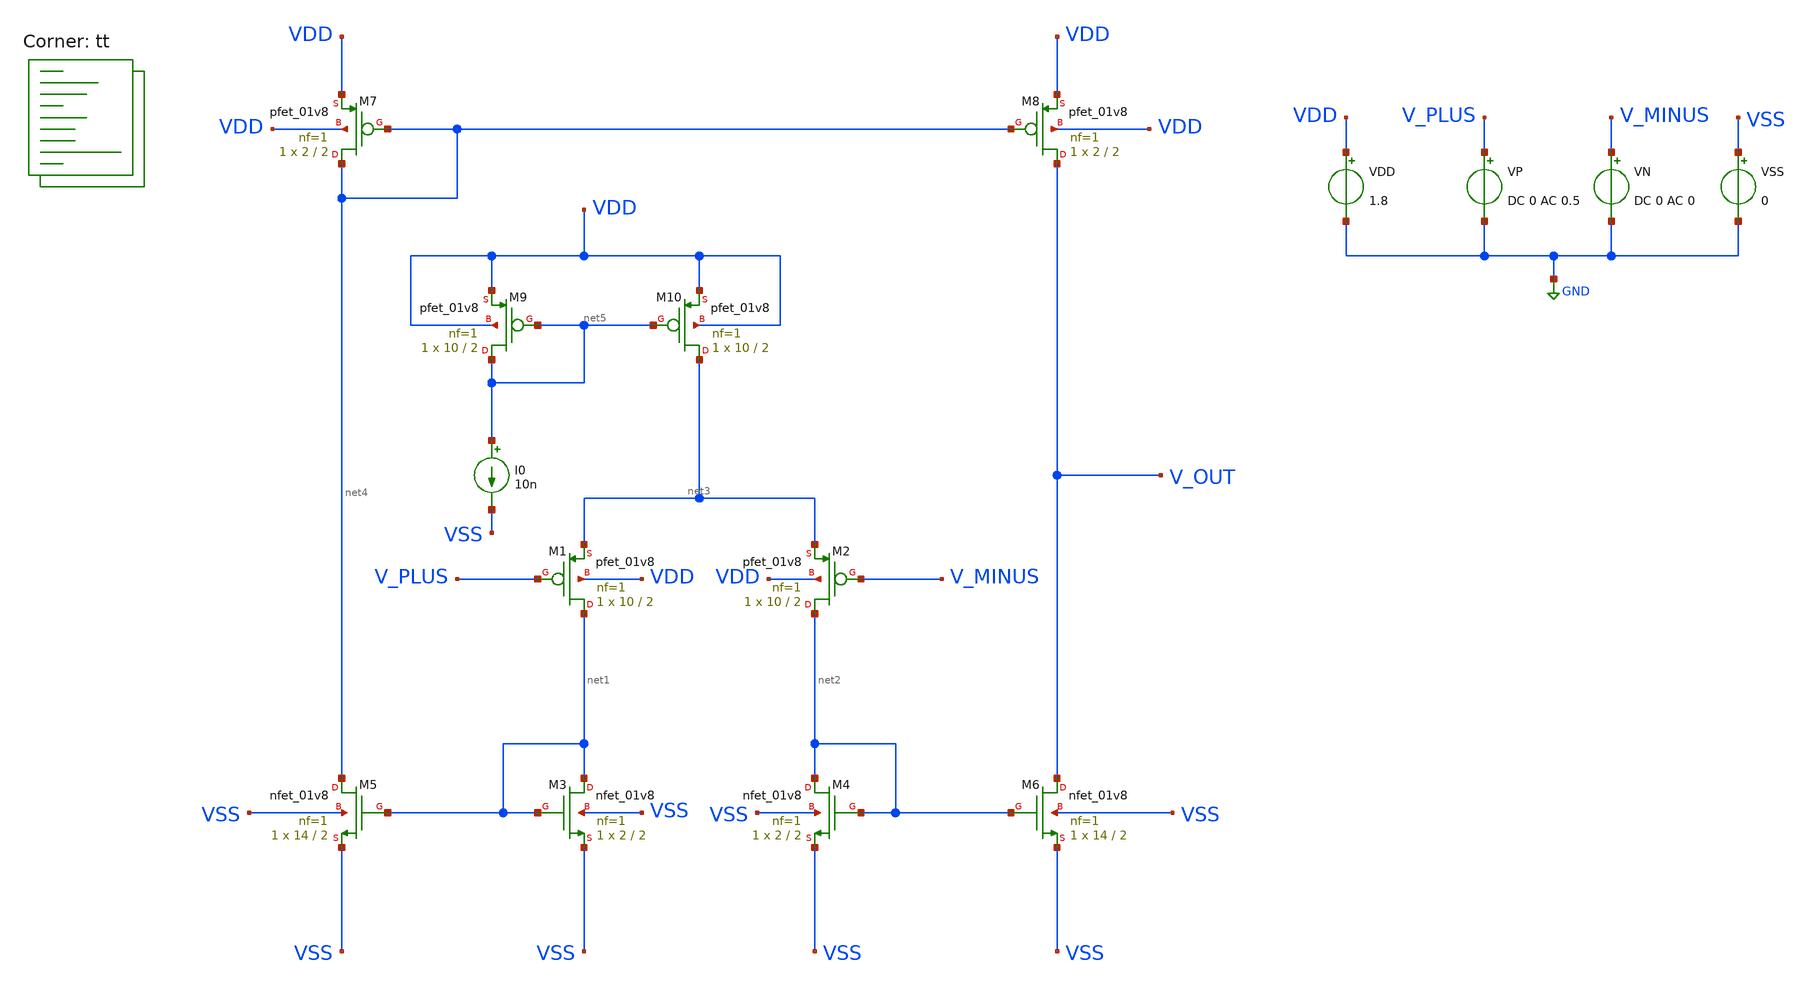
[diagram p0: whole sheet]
** sch_path: Schematic/OTA.sch
**.subckt OTA
XM1 net1 V_PLUS net3 VDD sky130_fd_pr__pfet_01v8 L=2 W=10 nf=1 ad='int((1 + 1)/2) * 10 / 1 * 0.29' as='int((1 + 2)/2) * 10 / 1 * 0.29'
+ pd='2*int((1 + 1)/2) * (10 / 1 + 0.29)' ps='2*int((1 + 2)/2) * (10 / 1 + 0.29)' nrd='0.29 / 10 ' nrs='0.29 / 10 '
+ sa=0 sb=0 sd=0 mult=1 m=1
XM3 net1 net1 VSS VSS sky130_fd_pr__nfet_01v8 L=2 W=2 nf=1 ad='int((1 + 1)/2) * 2 / 1 * 0.29' as='int((1 + 2)/2) * 2 / 1 * 0.29'
+ pd='2*int((1 + 1)/2) * (2 / 1 + 0.29)' ps='2*int((1 + 2)/2) * (2 / 1 + 0.29)' nrd='0.29 / 2 ' nrs='0.29 / 2 '
+ sa=0 sb=0 sd=0 mult=1 m=1
XM4 net2 net2 VSS VSS sky130_fd_pr__nfet_01v8 L=2 W=2 nf=1 ad='int((1 + 1)/2) * 2 / 1 * 0.29' as='int((1 + 2)/2) * 2 / 1 * 0.29'
+ pd='2*int((1 + 1)/2) * (2 / 1 + 0.29)' ps='2*int((1 + 2)/2) * (2 / 1 + 0.29)' nrd='0.29 / 2 ' nrs='0.29 / 2 '
+ sa=0 sb=0 sd=0 mult=1 m=1
XM2 net2 V_MINUS net3 VDD sky130_fd_pr__pfet_01v8 L=2 W=10 nf=1 ad='int((1 + 1)/2) * 10 / 1 * 0.29' as='int((1 + 2)/2) * 10 / 1 * 0.29'
+ pd='2*int((1 + 1)/2) * (10 / 1 + 0.29)' ps='2*int((1 + 2)/2) * (10 / 1 + 0.29)' nrd='0.29 / 10 ' nrs='0.29 / 10 '
+ sa=0 sb=0 sd=0 mult=1 m=1
XM5 net4 net1 VSS VSS sky130_fd_pr__nfet_01v8 L=2 W=14 nf=1 ad='int((1 + 1)/2) * 14 / 1 * 0.29' as='int((1 + 2)/2) * 14 / 1 * 0.29'
+ pd='2*int((1 + 1)/2) * (14 / 1 + 0.29)' ps='2*int((1 + 2)/2) * (14 / 1 + 0.29)' nrd='0.29 / 14 ' nrs='0.29 / 14 '
+ sa=0 sb=0 sd=0 mult=1 m=1
XM6 V_OUT net2 VSS VSS sky130_fd_pr__nfet_01v8 L=2 W=14 nf=1 ad='int((1 + 1)/2) * 14 / 1 * 0.29' as='int((1 + 2)/2) * 14 / 1 * 0.29'
+ pd='2*int((1 + 1)/2) * (14 / 1 + 0.29)' ps='2*int((1 + 2)/2) * (14 / 1 + 0.29)' nrd='0.29 / 14 ' nrs='0.29 / 14 '
+ sa=0 sb=0 sd=0 mult=1 m=1
XM7 net4 net4 VDD VDD sky130_fd_pr__pfet_01v8 L=2 W=2 nf=1 ad='int((1 + 1)/2) * 2 / 1 * 0.29' as='int((1 + 2)/2) * 2 / 1 * 0.29'
+ pd='2*int((1 + 1)/2) * (2 / 1 + 0.29)' ps='2*int((1 + 2)/2) * (2 / 1 + 0.29)' nrd='0.29 / 2 ' nrs='0.29 / 2 '
+ sa=0 sb=0 sd=0 mult=1 m=1
XM8 V_OUT net4 VDD VDD sky130_fd_pr__pfet_01v8 L=2 W=2 nf=1 ad='int((1 + 1)/2) * 2 / 1 * 0.29' as='int((1 + 2)/2) * 2 / 1 * 0.29'
+ pd='2*int((1 + 1)/2) * (2 / 1 + 0.29)' ps='2*int((1 + 2)/2) * (2 / 1 + 0.29)' nrd='0.29 / 2 ' nrs='0.29 / 2 '
+ sa=0 sb=0 sd=0 mult=1 m=1
XM10 net3 net5 VDD VDD sky130_fd_pr__pfet_01v8 L=2 W=10 nf=1 ad='int((1 + 1)/2) * 10 / 1 * 0.29' as='int((1 + 2)/2) * 10 / 1 * 0.29'
+ pd='2*int((1 + 1)/2) * (10 / 1 + 0.29)' ps='2*int((1 + 2)/2) * (10 / 1 + 0.29)' nrd='0.29 / 10 ' nrs='0.29 / 10 '
+ sa=0 sb=0 sd=0 mult=1 m=1
XM9 net5 net5 VDD VDD sky130_fd_pr__pfet_01v8 L=2 W=10 nf=1 ad='int((1 + 1)/2) * 10 / 1 * 0.29' as='int((1 + 2)/2) * 10 / 1 * 0.29'
+ pd='2*int((1 + 1)/2) * (10 / 1 + 0.29)' ps='2*int((1 + 2)/2) * (10 / 1 + 0.29)' nrd='0.29 / 10 ' nrs='0.29 / 10 '
+ sa=0 sb=0 sd=0 mult=1 m=1
I0 net5 VSS 10n
VDD VDD GND 1.8
VP V_PLUS GND DC 0 AC 0.5
VN V_MINUS GND DC 0 AC 0
VSS VSS GND 0
**** begin user architecture code
.lib $::SKYWATER_MODELS/sky130.lib.spice tt


.option savecurrents
.temp 27

.control
  save all
  op
  *dc VP 0 1.8 0.001

  ac dec 200 1 1e9

  plot db((v(v_out))/(v(v_plus)-v(v_minus))) ph((v(v_out))/(v(v_plus)-v(v_minus))) xlog

  *plot v(V_PLUS)-v(V_MINUS) v(V_OUT)
  *plot i(VDD)
.endc



**** end user architecture code
**.ends
.GLOBAL GND
.end
